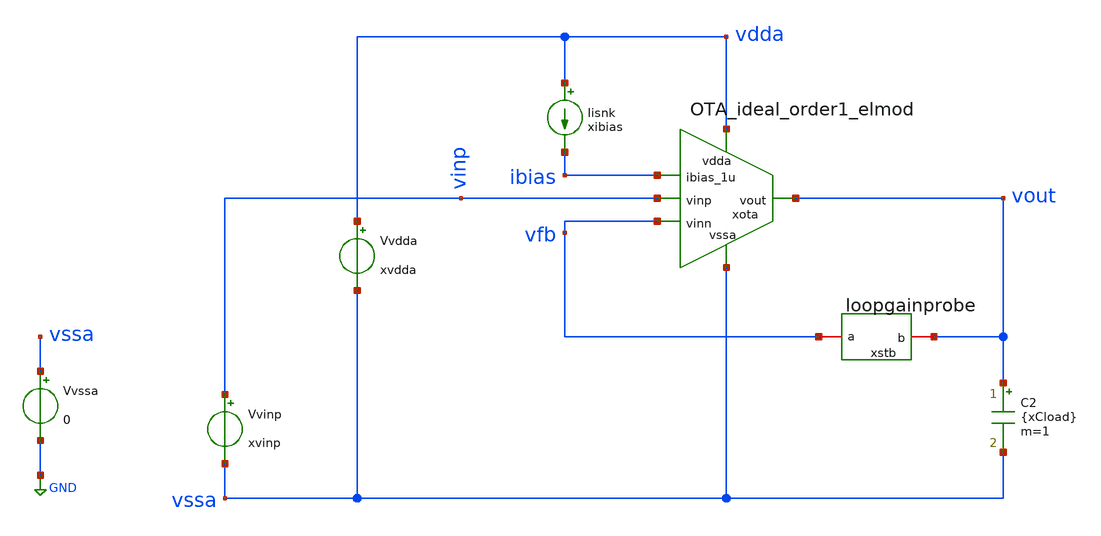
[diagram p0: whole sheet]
** sch_path: Running_closed_loop_stability_analysis_in_ngspice_through_xschem/tb_OTA_1stage.sch
**.subckt tb_OTA_1stage
Vvssa vssa GND 0
Vvdda vdda vssa xvdda
Vvinp vinp vssa xvinp
xota vdda vout vfb vinp ibias vssa OTA_ideal_order1_elmod
C2 vout vssa {xCload} m=1
xstb vfb vout loopgainprobe
Iisnk vdda ibias xibias
**** begin user architecture code

* Models
* Note: I name my nmos models as nmos and pmos ones as pmosx (just messing a bit)
.model nmos nmos level=54 version=4.8.2
.model pmosx pmos level=54 version=4.8.2

* Parameters
.param xvdda = 1.8
.param xvinp = 1
.param xibias = 2u
.param xCload = 0p
.param xgm_dp = 1e-3
.param xRin = 1/xgm_dp
.param xCout = 1p
.param xRout = 1e6

.model OTA_vcvs OTA_vcvs
* vlogA instantiation


  ** 1. DCOP analysis **
  ** must save the below for DCOP analysis to be back annotated onto the schematic
  .option savecurrents
  .save
  +  @m.xota.m1[vgs]
  +  @m.xota.m1[vth]
  +  @m.xota.m1[gds]
  +  @m.xota.m1[gm]
  +  @m.xota.m1[id]
  +  @m.xota2.m1[vgs]
  +  @m.xota2.m1[vth]
  +  @m.xota2.m1[gds]
  +  @m.xota2.m1[gm]
  +  @m.xota2.m1[id]

  +  @m.xota.m2[vgs]
  +  @m.xota.m2[vth]
  +  @m.xota.m2[gds]
  +  @m.xota.m2[gm]
  +  @m.xota.m2[id]
  +  @m.xota2.m2[vgs]
  +  @m.xota2.m2[vth]
  +  @m.xota2.m2[gds]
  +  @m.xota2.m2[gm]
  +  @m.xota2.m2[id]

  +  @m.xota.m3[vgs]
  +  @m.xota.m3[vth]
  +  @m.xota.m3[gds]
  +  @m.xota.m3[gm]
  +  @m.xota.m3[id]
  +  @m.xota2.m3[vgs]
  +  @m.xota2.m3[vth]
  +  @m.xota2.m3[gds]
  +  @m.xota2.m3[gm]
  +  @m.xota2.m3[id]

  +  @m.xota.m4[vgs]
  +  @m.xota.m4[vth]
  +  @m.xota.m4[gds]
  +  @m.xota.m4[gm]
  +  @m.xota.m4[id]
  +  @m.xota2.m4[vgs]
  +  @m.xota2.m4[vth]
  +  @m.xota2.m4[gds]
  +  @m.xota2.m4[gm]
  +  @m.xota2.m4[id]

  +  @m.xota.m5[vgs]
  +  @m.xota.m5[vth]
  +  @m.xota.m5[gds]
  +  @m.xota.m5[gm]
  +  @m.xota.m5[id]
  +  @m.xota2.m5[vgs]
  +  @m.xota2.m5[vth]
  +  @m.xota2.m5[gds]
  +  @m.xota2.m5[gm]
  +  @m.xota2.m5[id]

  +  @m.xota.m6[vgs]
  +  @m.xota.m6[vth]
  +  @m.xota.m6[gds]
  +  @m.xota.m6[gm]
  +  @m.xota.m6[id]
  +  @m.xota2.m6vgs]
  +  @m.xota2.m6[vth]
  +  @m.xota2.m6[gds]
  +  @m.xota2.m6[gm]
  +  @m.xota2.m6[id]

  .control
  pre_osdi OTA_vcvs.osdi
  save all

  op
  write tb_ota_1stage_op.raw

** 2. AC ANALYSIS **

  alter i.xstb.Ii acmag=0
  alter v.xstb.Vi acmag=1

  ac dec 10 1 100G
  remzerovec
  write tb_OTA_1stage_ac1.raw

  alter i.xstb.Ii acmag=1
  alter v.xstb.Vi acmag=0

  ac dec 10 1 10G

  * use this line if you want the phase response to start at 180deg
  *let av = {1/(1-1/(2*(ac1.i(v.xstb.Vi)*ac2.v(xstb.x)-ac1.v(xstb.x)*ac2.i(v.xstb.Vi))+ac1.v(xstb.x)+ac2.i(v.xstb.Vi)))}

  * use this line if you want the phase response to start at 0deg (more conventional and directly
+ corresponds to Franks derivation)
  let av = {1/(1/(2*(ac1.i(v.xstb.Vi)*ac2.v(xstb.x)-ac1.v(xstb.x)*ac2.i(v.xstb.Vi))+ac1.v(xstb.x)+ac2.i(v.xstb.Vi))-1)}

  remzerovec
  write tb_OTA_1stage_ac2.raw

  *ngspice plots
  *plot vdb(av) xlog
  *plot {(180/pi)*vp(av)} xlog
  *plot 180*cph(av)/pi

  ** 3. MEASURES **

  let n45_rads = -45*(pi/180)
  meas AC Av_0 FIND vdb(av) AT=10
  echo --
  meas AC BW WHEN vp(av)=n45_rads CROSS=1
  echo --
  meas AC Av_BW FIND vdb(av) WHEN vp(av)=n45_rads CROSS=1
  echo --
  meas AC ULGF WHEN vdb(av)=0
  echo --
  meas AC ULGF_phi_rads FIND vp(av) WHEN vdb(av)=0 CROSS=1
  let ULGF_phi_deg = ULGF_phi_rads*(180/pi)
  print ULGF_phi_deg
  let PM = 180+ULGF_phi_deg
  print PM
  echo --
  * putting in -170 since this is a 2nd-order system so doesnt ever achieve -180
  let n180_rads = -170*(pi/180)
  meas AC GM FIND vdb(av) WHEN vp(av)=n180_rads CROSS=1

  setplot

.endc


**** end user architecture code
**.ends

* expanding   symbol:  OTA_ideal_order1_elmod.sym # of pins=6
** sym_path: Running_vloga_in_ngspice/OTA.sym
** sch_path: Running_vloga_in_ngspice/OTA_ideal_order1_elmod.sch
.subckt OTA_ideal_order1_elmod vdda vout vinn vinp ibias_1u vssa
*.ipin vssa
*.ipin vinp
*.ipin ibias_1u
*.ipin vinn
*.ipin vdda
*.opin vout
E1 net1 vssa vinp vinn 1
R1 net2 vssa {xRin} m=1
F1 vdda net3 Vidp 1
Vidp net1 net2 0
R2 vout vssa {xRout} m=1
C2 vout vssa {xCout} m=1
Viout net3 vout 0
R3 ibias_1u vssa 1MEG m=1
.ends


* expanding   symbol:  loopgainprobe.sym # of pins=2
** sym_path: tb_OTA_1stage_ihp/loopgainprobe.sym
** sch_path: tb_OTA_1stage_ihp/loopgainprobe.sch
.subckt loopgainprobe a b
*.iopin b
*.iopin a
**** begin user architecture code
Ii 0 x DC 0 AC 0
Vi x a DC 0 AC 1
Vnodebuffer b x 0
**** end user architecture code
.ends

.GLOBAL GND
.end
